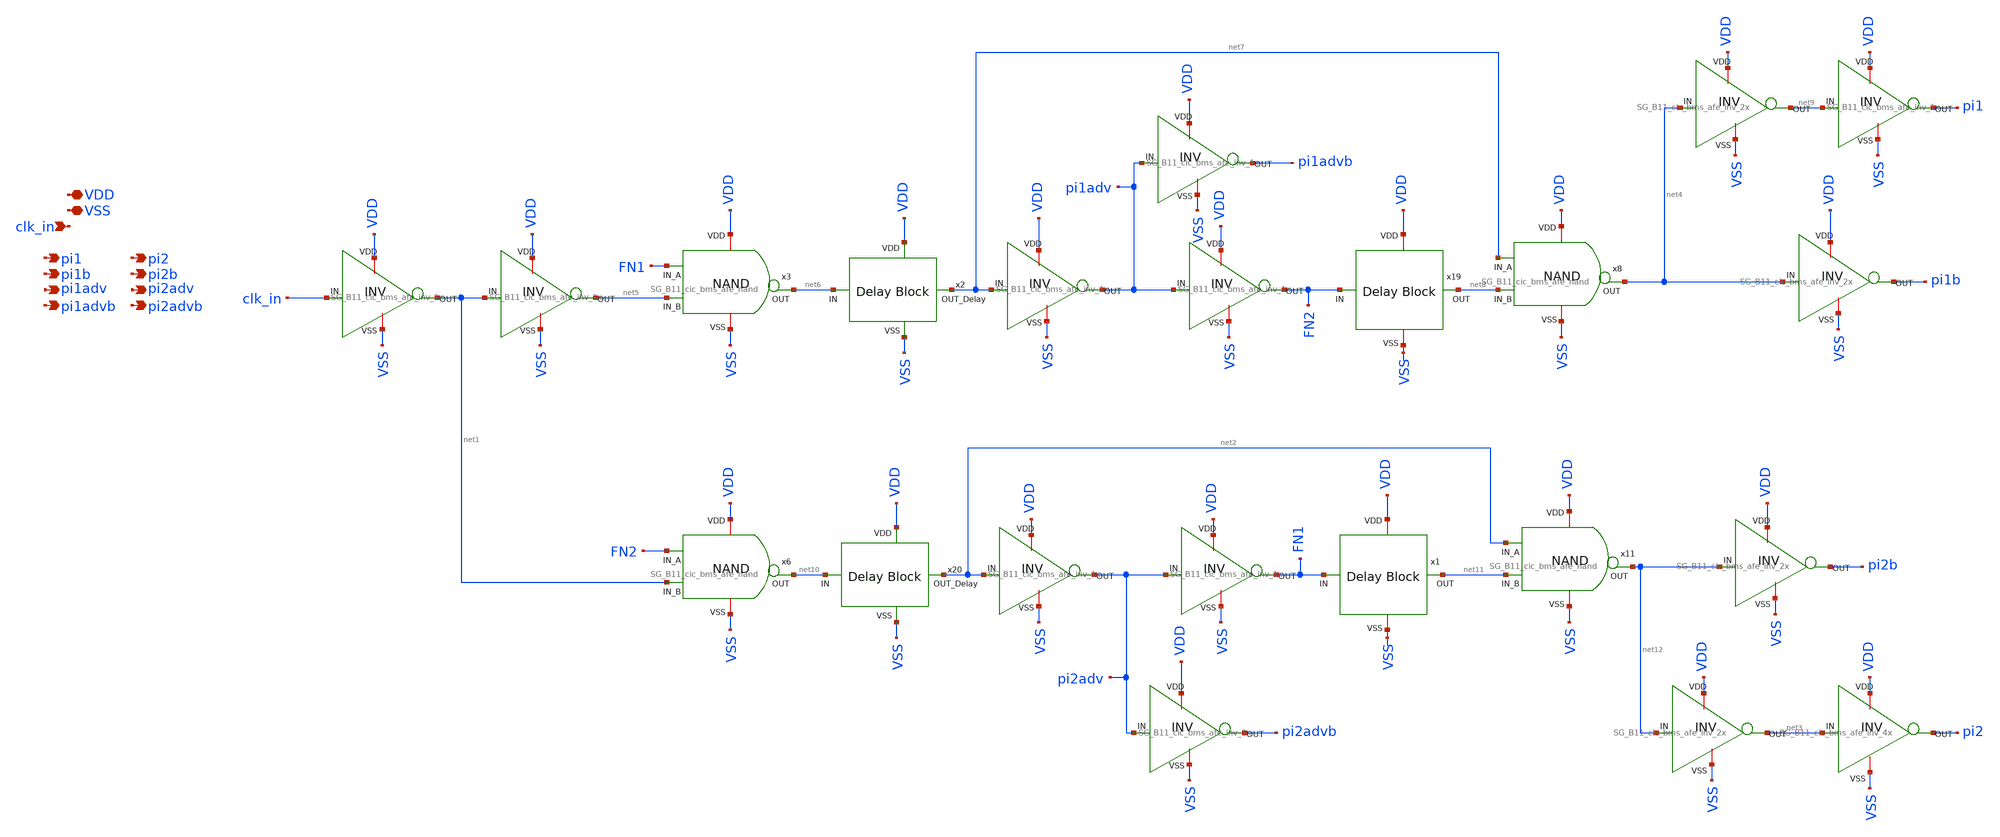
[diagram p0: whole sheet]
** sch_path: design/schematics/NOCG/SG_B11_cic_bms_afe_non_overlapping_clk.sch
**.subckt SG_B11_cic_bms_afe_non_overlapping_clk pi1b pi2b clk_in pi1advb pi2advb pi1adv pi2adv pi1
*+ pi2 VDD VSS
*.opin pi1b
*.opin pi2b
*.ipin clk_in
*.opin pi1advb
*.opin pi2advb
*.opin pi1adv
*.opin pi2adv
*.opin pi1
*.opin pi2
*.iopin VDD
*.iopin VSS
x7 VDD net1 clk_in VSS SG_B11_cic_bms_afe_inv_1x
x15 VDD pi1adv net7 VSS SG_B11_cic_bms_afe_inv_1x
x16 VDD FN2 pi1adv VSS SG_B11_cic_bms_afe_inv_1x
x17 VDD pi1advb pi1adv VSS SG_B11_cic_bms_afe_inv_1x
x4 VDD pi1 net9 VSS SG_B11_cic_bms_afe_inv_1x
x18 VDD pi2adv net2 VSS SG_B11_cic_bms_afe_inv_1x
x21 VDD FN1 pi2adv VSS SG_B11_cic_bms_afe_inv_1x
x22 VDD pi2advb pi2adv VSS SG_B11_cic_bms_afe_inv_1x
x3 VDD net5 FN1 net6 VSS SG_B11_cic_bms_afe_nand
x19 VDD FN2 net8 VSS SG_B11_cic_bms_afe_delay_block_3n
x1 VDD FN1 net11 VSS SG_B11_cic_bms_afe_delay_block_3n
x2 VDD net7 net6 VSS SG_B11_cic_bms_afe_delay_block_5V
x5 VDD net4 net9 VSS SG_B11_cic_bms_afe_inv_2x
x9 VDD net4 pi1b VSS SG_B11_cic_bms_afe_inv_2x
x10 VDD net12 pi2b VSS SG_B11_cic_bms_afe_inv_2x
x13 VDD net12 net3 VSS SG_B11_cic_bms_afe_inv_2x
x14 VDD net3 pi2 VSS SG_B11_cic_bms_afe_inv_4x
x12 VDD net5 net1 VSS SG_B11_cic_bms_afe_inv_1x
x6 VDD net1 FN2 net10 VSS SG_B11_cic_bms_afe_nand
x20 VDD net2 net10 VSS SG_B11_cic_bms_afe_delay_block_5V
x8 VDD net8 net7 net4 VSS SG_B11_cic_bms_afe_nand
x11 VDD net11 net2 net12 VSS SG_B11_cic_bms_afe_nand
**.ends
.end
